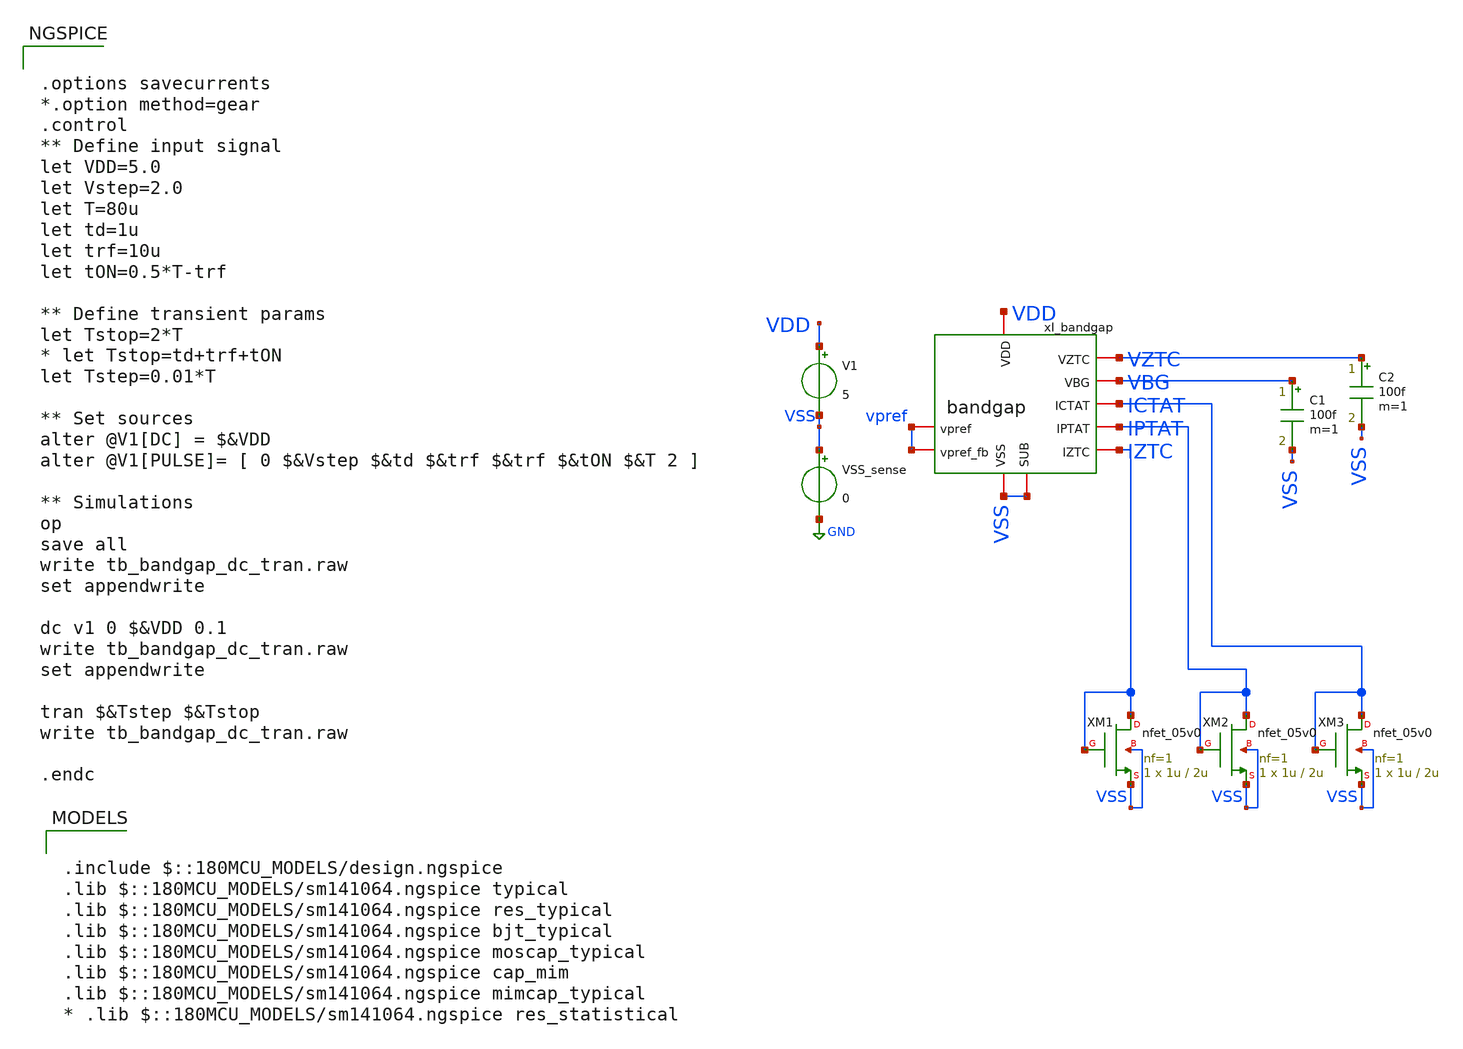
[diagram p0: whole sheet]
** sch_path: designs/libs/tb_bandgap/tb_bandgap_dc_tran/tb_bandgap_dc_tran.sch
**.subckt tb_bandgap_dc_tran
V1 VDD VSS 5
VSS_sense VSS GND 0
C1 VBG VSS 100f m=1
xI_bandgap VDD VBG IPTAT IZTC VSS VSS vpref vpref ICTAT VZTC bandgap
C2 VZTC VSS 100f m=1
XM1 IZTC IZTC VSS VSS nfet_05v0 L=2u W=1u nf=1 ad='int((nf+1)/2) * W/nf * 0.18u' as='int((nf+2)/2) * W/nf * 0.18u'
+ pd='2*int((nf+1)/2) * (W/nf + 0.18u)' ps='2*int((nf+2)/2) * (W/nf + 0.18u)' nrd='0.18u / W' nrs='0.18u / W'
+ sa=0 sb=0 sd=0 m=1
XM2 IPTAT IPTAT VSS VSS nfet_05v0 L=2u W=1u nf=1 ad='int((nf+1)/2) * W/nf * 0.18u' as='int((nf+2)/2) * W/nf * 0.18u'
+ pd='2*int((nf+1)/2) * (W/nf + 0.18u)' ps='2*int((nf+2)/2) * (W/nf + 0.18u)' nrd='0.18u / W' nrs='0.18u / W'
+ sa=0 sb=0 sd=0 m=1
XM3 ICTAT ICTAT VSS VSS nfet_05v0 L=2u W=1u nf=1 ad='int((nf+1)/2) * W/nf * 0.18u' as='int((nf+2)/2) * W/nf * 0.18u'
+ pd='2*int((nf+1)/2) * (W/nf + 0.18u)' ps='2*int((nf+2)/2) * (W/nf + 0.18u)' nrd='0.18u / W' nrs='0.18u / W'
+ sa=0 sb=0 sd=0 m=1
**** begin user architecture code

.include $::180MCU_MODELS/design.ngspice
.lib $::180MCU_MODELS/sm141064.ngspice typical
.lib $::180MCU_MODELS/sm141064.ngspice res_typical
.lib $::180MCU_MODELS/sm141064.ngspice bjt_typical
.lib $::180MCU_MODELS/sm141064.ngspice moscap_typical
.lib $::180MCU_MODELS/sm141064.ngspice cap_mim
.lib $::180MCU_MODELS/sm141064.ngspice mimcap_typical
* .lib $::180MCU_MODELS/sm141064.ngspice res_statistical



.options savecurrents
*.option method=gear
.control
** Define input signal
let VDD=5.0
let Vstep=2.0
let T=80u
let td=1u
let trf=10u
let tON=0.5*T-trf

** Define transient params
let Tstop=2*T
* let Tstop=td+trf+tON
let Tstep=0.01*T

** Set sources
alter @V1[DC] = $&VDD
alter @V1[PULSE]= [ 0 $&Vstep $&td $&trf $&trf $&tON $&T 2 ]

** Simulations
op
save all
write tb_bandgap_dc_tran.raw
set appendwrite

dc v1 0 $&VDD 0.1
write tb_bandgap_dc_tran.raw
set appendwrite

tran $&Tstep $&Tstop
write tb_bandgap_dc_tran.raw

.endc


**** end user architecture code
**.ends
.GLOBAL GND
.end
